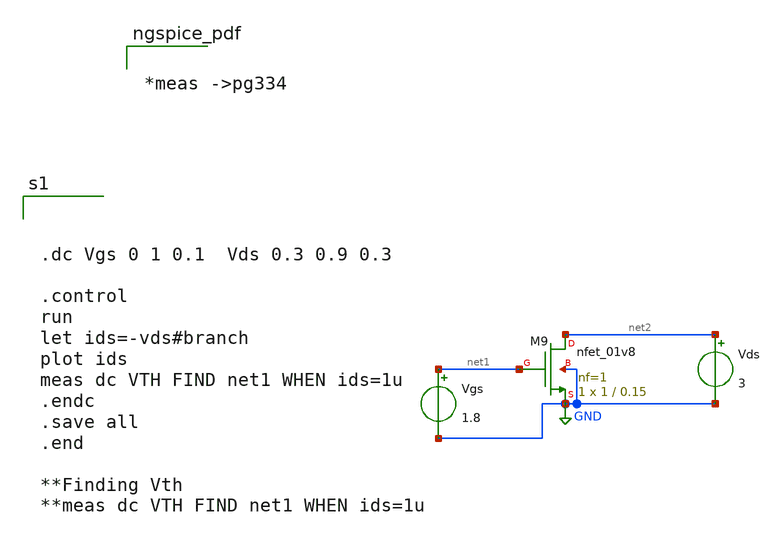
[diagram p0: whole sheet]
** sch_path: nfet_char.sch
**.subckt nfet_char
XM9 net2 net1 GND GND sky130_fd_pr__nfet_01v8 L=0.15 W=1 nf=1 ad='int((1 + 1)/2) * 1 / 1 * 0.29' as='int((1 + 2)/2) * 1 / 1 * 0.29'
+ pd='2*int((1 + 1)/2) * (1 / 1 + 0.29)' ps='2*int((1 + 2)/2) * (1 / 1 + 0.29)' nrd='0.29 / 1 ' nrs='0.29 / 1 '
+ sa=0 sb=0 sd=0 mult=1 m=1
Vgs net1 GND 1.8
Vds net2 GND 3
**** begin user architecture code



.dc Vgs 0 1 0.1  Vds 0.3 0.9 0.3

.control
run
let ids=-vds#branch
plot ids
meas dc VTH FIND net1 WHEN ids=1u
.endc
.save all
.end

**Finding Vth
**meas dc VTH FIND net1 WHEN ids=1u



** opencircuitdesign pdks install
.lib $::SKYWATER_MODELS/sky130.lib.spice tt



*meas ->pg334


**** end user architecture code
**.ends
.GLOBAL GND
.end
